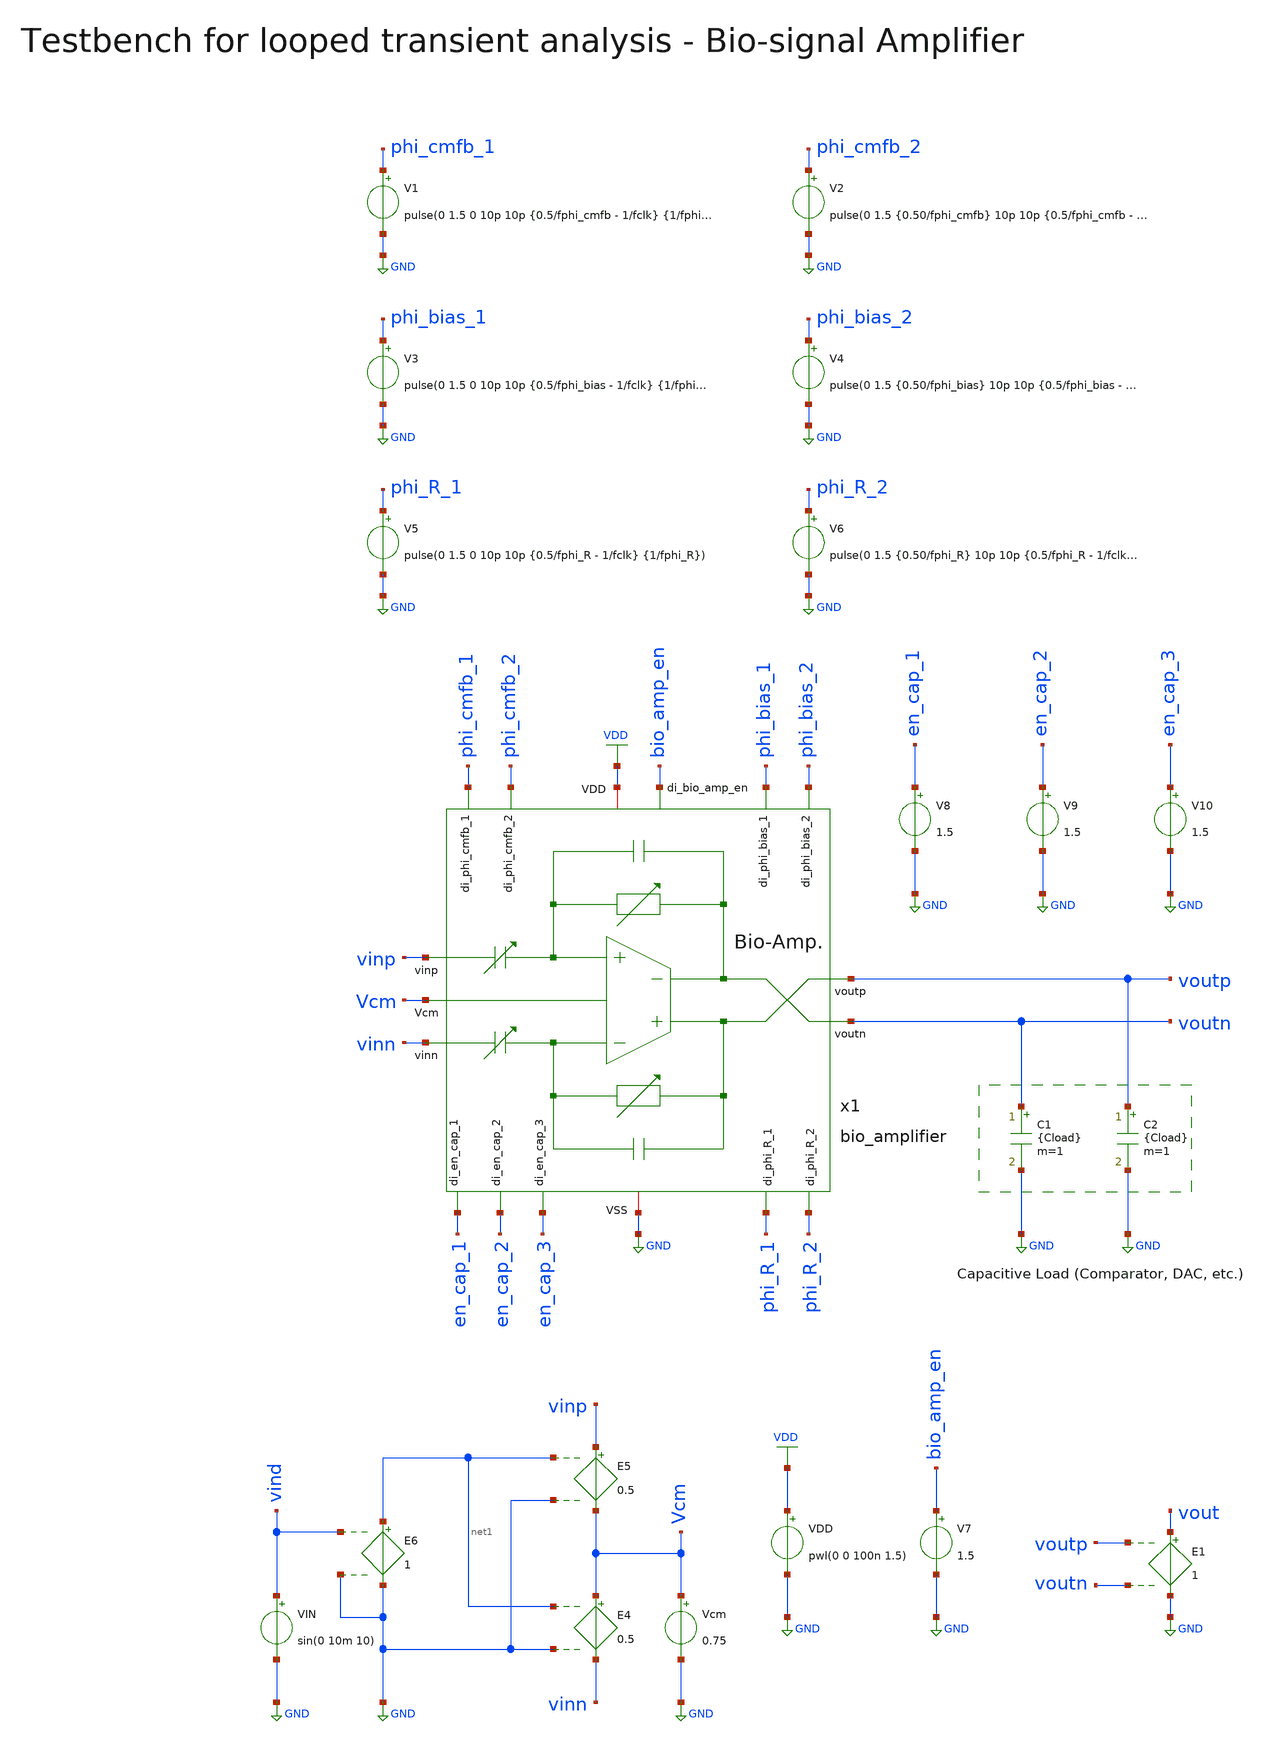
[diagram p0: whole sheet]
** sch_path: SG13G2_ATBS-ADC-main/xschem/bio_amplifier/testbenches/bio_amplifier_tb_looped_tran_cl.sch
**.subckt bio_amplifier_tb_looped_tran_cl
C1 voutn GND {Cload} m=1
C2 voutp GND {Cload} m=1
Vcm Vcm GND 0.75
E4 Vcm vinn net1 GND 0.5
E5 vinp Vcm net1 GND 0.5
E6 net1 GND vind GND 1
V7 bio_amp_en GND 1.5
V8 en_cap_1 GND 1.5
V9 en_cap_2 GND 1.5
V10 en_cap_3 GND 1.5
VIN vind GND sin(0 10m 10)
E1 vout GND voutp voutn 1
x1 phi_bias_2 phi_bias_1 phi_R_2 phi_R_1 en_cap_3 en_cap_1 en_cap_2 phi_cmfb_2 phi_cmfb_1 voutp
+ bio_amp_en vinp Vcm voutn vinn VDD GND bio_amplifier
VDD VDD GND pwl(0 0 100n 1.5)
V1 phi_cmfb_1 GND pulse(0 1.5 0 10p 10p {0.5/fphi_cmfb - 1/fclk} {1/fphi_cmfb})
V2 phi_cmfb_2 GND pulse(0 1.5 {0.50/fphi_cmfb} 10p 10p {0.5/fphi_cmfb - 1/fclk} {1/fphi_cmfb})
V3 phi_bias_1 GND pulse(0 1.5 0 10p 10p {0.5/fphi_bias - 1/fclk} {1/fphi_bias})
V4 phi_bias_2 GND pulse(0 1.5 {0.50/fphi_bias} 10p 10p {0.5/fphi_bias - 1/fclk} {1/fphi_bias})
V5 phi_R_1 GND pulse(0 1.5 0 10p 10p {0.5/fphi_R - 1/fclk} {1/fphi_R})
V6 phi_R_2 GND pulse(0 1.5 {0.50/fphi_R} 10p 10p {0.5/fphi_R - 1/fclk} {1/fphi_R})
**** begin user architecture code


.param temp=27
.param fclk=8000000
.csparam fclk=fclk
.param fphi_cmfb=62500
.param fphi_bias=62500
.param fphi_R=7810
* 227.56fF DAC
.param Cload=227.56f
.options savecurrents reltol=1e-2 abstol=1e-12 gmin=1e-12
.control

* optran 0 0 0 1u 1m 0
* save all
save vind vinp vinn voutp voutn vout x1.x1.Vbias x1.x1.Vbiasc
save phi_cmfb_1 phi_cmfb_2 phi_bias_1 phi_bias_2 phi_R_1 phi_R_2 en_cap_1 en_cap_2 en_cap_3
setplot const
set wr_vecnames
set wr_singlescale

* User constants
let fstart = 1k
let fstop = 100k
let amount_of_periods = 2
let points_per_period = 5
let points_per_dec = 1
let vamp = 0.001

* Generate a logarithmic frequency vector
compose freq_vec dec=$&const.points_per_dec start=$&const.fstart stop=$&const.fstop

* Generate gain and phase vectors
let Acl_dB_vec = freq_vec
let phase_vec = freq_vec

* Loop index
let idx = 0

* For-Loop
foreach freq_val $&freq_vec
  * 10 data points per period
  * let tstep = 1/($&const.points_per_period*$freq_val)
  let tstep = 1/fclk

  * 2 periods long
  let tstop = $&const.amount_of_periods * 1/$freq_val

  * Alter input sine frequency
  alter @VIN[SIN] = [ 0 $&const.vamp $freq_val 0 0 0 ]

  * Transient Analysis
  tran $&tstep $&tstop
  write bio_amplifier_tb_looped_tran_cl.raw
  set appendwrite

  * Measure maximum voltage of input
  meas tran vind_peak_peak PP v(vind)
  let vind_peak = vind_peak_peak / 2

  * Measure time at maximum voltage of input
  meas tran t_vind_peak MAX_AT v(vind)

  * Measure maximum voltage of output
  meas tran vout_peak_peak PP v(vout)
  let vout_peak = vout_peak_peak / 2

  * Measure time at maximum voltage of output
  meas tran t_vout_peak MAX_AT v(vout)

  * Calculate gain
  let Acl = vout_peak / vind_peak
  let Acl_dB = vdb(Acl)

  * Calculate phase
  let phase = (t_vout_peak - t_vind_peak) * $freq_val * 360

  * Append to vector
  let const.Acl_dB_vec[const.idx] = Acl_dB
  let const.phase_vec[const.idx] = phase

  * Update index
  let const.idx = const.idx + 1
  echo ======================================================
end

print const.Acl_dB_vec
print const.phase_vec

* Setscale for plot against frequency
setscale const.Acl_dB_vec const.freq_vec
setscale const.phase_vec const.freq_vec

* Plot closed-loop gain and phase vs. frequency
plot xlog const.Acl_dB_vec title 'Closed-loop gain' ylabel 'dB'
plot xlog const.phase_vec title 'Phase' ylabel 'deg'

* Write Data
wrdata
+ /foss/designs/SG13G2_ATBS-ADC-main/python/plot_simulations/data/bio_amplifier_tb_looped_tran_cl.txt v(const.Acl_dB_vec) v(const.phase_vec)

*quit
.endc



.lib cornerMOSlv.lib mos_tt
.lib cornerMOShv.lib mos_tt
.lib cornerRES.lib res_typ

**** end user architecture code
**.ends
.GLOBAL GND
.GLOBAL VDD
.end
